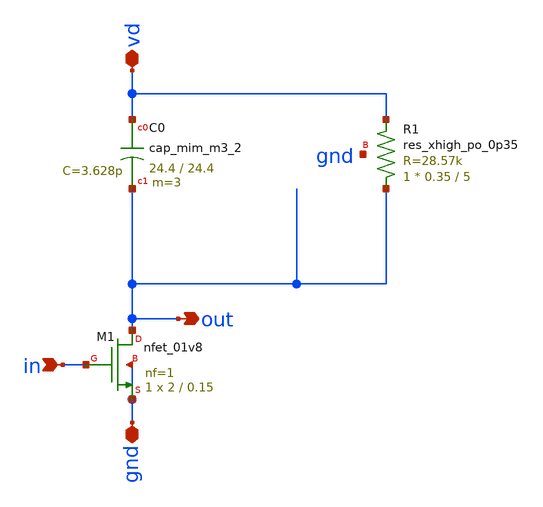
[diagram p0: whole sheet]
** sch_path: ask_modulator/xschem/ask-modulator.sch
**.subckt ask-modulator gnd in out vd
*.iopin gnd
*.ipin in
*.opin out
*.iopin vd
XC0 vd out sky130_fd_pr__cap_mim_m3_2 W=24.4 L=24.4 MF=3 m=3
XR1 net1 vd gnd sky130_fd_pr__res_xhigh_po_0p35 L=5 mult=1 m=1
XM1 out in gnd gnd sky130_fd_pr__nfet_01v8 L=0.15 W=2 nf=1 ad='int((nf+1)/2) * W/nf * 0.29' as='int((nf+2)/2) * W/nf * 0.29'
+ pd='2*int((nf+1)/2) * (W/nf + 0.29)' ps='2*int((nf+2)/2) * (W/nf + 0.29)' nrd='0.29 / W' nrs='0.29 / W'
+ sa=0 sb=0 sd=0 mult=1 m=1
**.ends
.end
